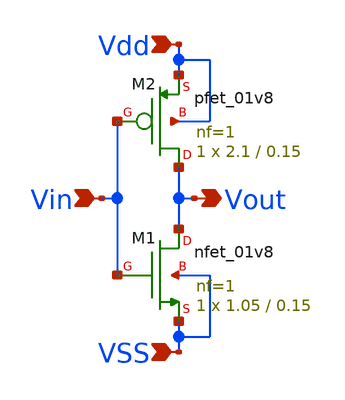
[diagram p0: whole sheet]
** sch_path: xschem files/inv_1.sch
**.subckt inv_1 Vdd VSS Vout Vin
*.ipin Vdd
*.ipin VSS
*.opin Vout
*.ipin Vin
XM1 Vout Vin VSS VSS sky130_fd_pr__nfet_01v8 L=0.15 W=1.05 nf=1 ad='int((nf+1)/2) * W/nf * 0.29' as='int((nf+2)/2) * W/nf * 0.29'
+ pd='2*int((nf+1)/2) * (W/nf + 0.29)' ps='2*int((nf+2)/2) * (W/nf + 0.29)' nrd='0.29 / W' nrs='0.29 / W'
+ sa=0 sb=0 sd=0 mult=1 m=1
XM2 Vout Vin Vdd Vdd sky130_fd_pr__pfet_01v8 L=0.15 W=2.1 nf=1 ad='int((nf+1)/2) * W/nf * 0.29' as='int((nf+2)/2) * W/nf * 0.29'
+ pd='2*int((nf+1)/2) * (W/nf + 0.29)' ps='2*int((nf+2)/2) * (W/nf + 0.29)' nrd='0.29 / W' nrs='0.29 / W'
+ sa=0 sb=0 sd=0 mult=1 m=1
**.ends
.end
